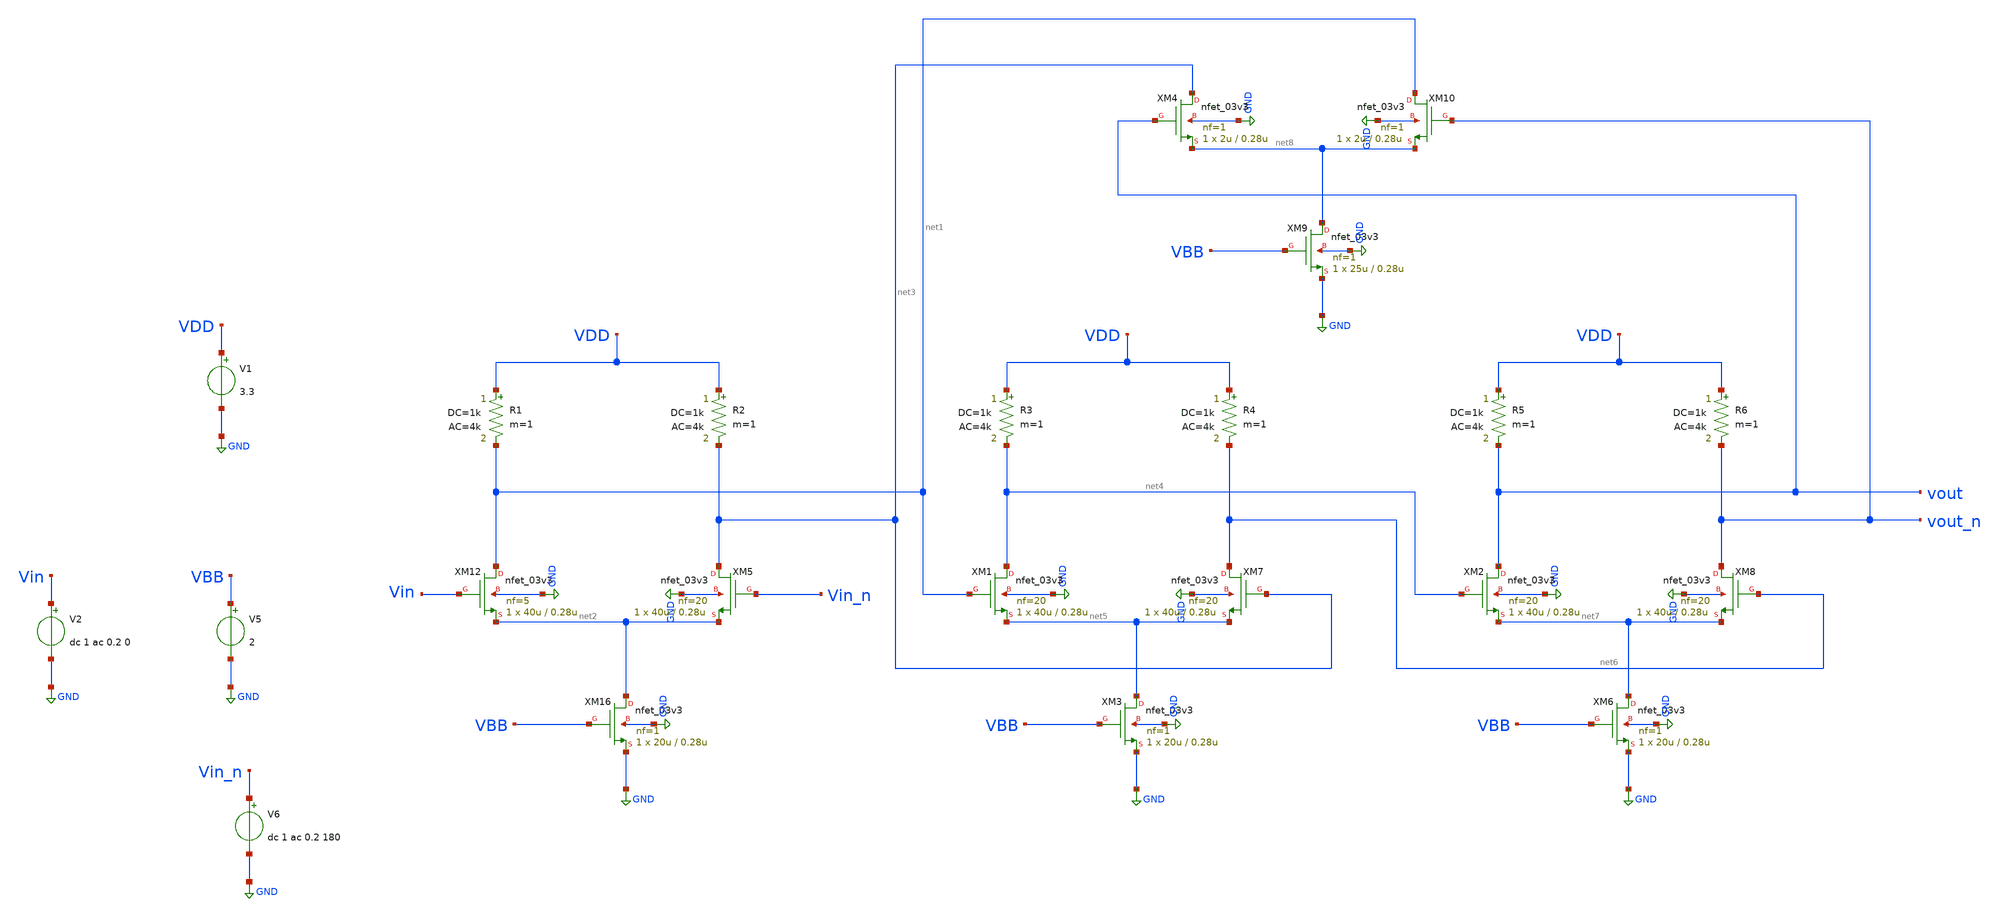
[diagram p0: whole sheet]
** sch_path: blocks/vga/fgas/untitled-4.sch
**.subckt untitled-4
XM12 net1 Vin net2 GND nfet_03v3 L=0.28u W=40u nf=5 ad='int((nf+1)/2) * W/nf * 0.18u' as='int((nf+2)/2) * W/nf * 0.18u'
+ pd='2*int((nf+1)/2) * (W/nf + 0.18u)' ps='2*int((nf+2)/2) * (W/nf + 0.18u)' nrd='0.18u / W' nrs='0.18u / W'
+ sa=0 sb=0 sd=0 m=1
XM16 net2 VBB GND GND nfet_03v3 L=0.28u W=20u nf=1 ad='int((nf+1)/2) * W/nf * 0.18u' as='int((nf+2)/2) * W/nf * 0.18u'
+ pd='2*int((nf+1)/2) * (W/nf + 0.18u)' ps='2*int((nf+2)/2) * (W/nf + 0.18u)' nrd='0.18u / W' nrs='0.18u / W'
+ sa=0 sb=0 sd=0 m=1
V1 VDD GND 3.3
V2 Vin GND dc 1 ac 0.2 0
V6 Vin_n GND dc 1 ac 0.2 180
V5 VBB GND 2
R1 VDD net1 1k ac=4k m=1
R2 VDD net3 1k ac=4k m=1
XM3 net5 VBB GND GND nfet_03v3 L=0.28u W=20u nf=1 ad='int((nf+1)/2) * W/nf * 0.18u' as='int((nf+2)/2) * W/nf * 0.18u'
+ pd='2*int((nf+1)/2) * (W/nf + 0.18u)' ps='2*int((nf+2)/2) * (W/nf + 0.18u)' nrd='0.18u / W' nrs='0.18u / W'
+ sa=0 sb=0 sd=0 m=1
R3 VDD net4 1k ac=4k m=1
R4 VDD net6 1k ac=4k m=1
XM6 net7 VBB GND GND nfet_03v3 L=0.28u W=20u nf=1 ad='int((nf+1)/2) * W/nf * 0.18u' as='int((nf+2)/2) * W/nf * 0.18u'
+ pd='2*int((nf+1)/2) * (W/nf + 0.18u)' ps='2*int((nf+2)/2) * (W/nf + 0.18u)' nrd='0.18u / W' nrs='0.18u / W'
+ sa=0 sb=0 sd=0 m=1
R5 VDD vout 1k ac=4k m=1
R6 VDD vout_n 1k ac=4k m=1
XM9 net8 VBB GND GND nfet_03v3 L=0.28u W=25u nf=1 ad='int((nf+1)/2) * W/nf * 0.18u' as='int((nf+2)/2) * W/nf * 0.18u'
+ pd='2*int((nf+1)/2) * (W/nf + 0.18u)' ps='2*int((nf+2)/2) * (W/nf + 0.18u)' nrd='0.18u / W' nrs='0.18u / W'
+ sa=0 sb=0 sd=0 m=1
XM1 net4 net1 net5 GND nfet_03v3 L=0.28u W=40u nf=20 ad='int((nf+1)/2) * W/nf * 0.18u' as='int((nf+2)/2) * W/nf * 0.18u'
+ pd='2*int((nf+1)/2) * (W/nf + 0.18u)' ps='2*int((nf+2)/2) * (W/nf + 0.18u)' nrd='0.18u / W' nrs='0.18u / W'
+ sa=0 sb=0 sd=0 m=1
XM2 vout net4 net7 GND nfet_03v3 L=0.28u W=40u nf=20 ad='int((nf+1)/2) * W/nf * 0.18u' as='int((nf+2)/2) * W/nf * 0.18u'
+ pd='2*int((nf+1)/2) * (W/nf + 0.18u)' ps='2*int((nf+2)/2) * (W/nf + 0.18u)' nrd='0.18u / W' nrs='0.18u / W'
+ sa=0 sb=0 sd=0 m=1
XM4 net3 vout net8 GND nfet_03v3 L=0.28u W=2u nf=1 ad='int((nf+1)/2) * W/nf * 0.18u' as='int((nf+2)/2) * W/nf * 0.18u'
+ pd='2*int((nf+1)/2) * (W/nf + 0.18u)' ps='2*int((nf+2)/2) * (W/nf + 0.18u)' nrd='0.18u / W' nrs='0.18u / W'
+ sa=0 sb=0 sd=0 m=1
XM5 net3 Vin_n net2 GND nfet_03v3 L=0.28u W=40u nf=20 ad='int((nf+1)/2) * W/nf * 0.18u' as='int((nf+2)/2) * W/nf * 0.18u'
+ pd='2*int((nf+1)/2) * (W/nf + 0.18u)' ps='2*int((nf+2)/2) * (W/nf + 0.18u)' nrd='0.18u / W' nrs='0.18u / W'
+ sa=0 sb=0 sd=0 m=1
XM7 net6 net3 net5 GND nfet_03v3 L=0.28u W=40u nf=20 ad='int((nf+1)/2) * W/nf * 0.18u' as='int((nf+2)/2) * W/nf * 0.18u'
+ pd='2*int((nf+1)/2) * (W/nf + 0.18u)' ps='2*int((nf+2)/2) * (W/nf + 0.18u)' nrd='0.18u / W' nrs='0.18u / W'
+ sa=0 sb=0 sd=0 m=1
XM8 vout_n net6 net7 GND nfet_03v3 L=0.28u W=40u nf=20 ad='int((nf+1)/2) * W/nf * 0.18u' as='int((nf+2)/2) * W/nf * 0.18u'
+ pd='2*int((nf+1)/2) * (W/nf + 0.18u)' ps='2*int((nf+2)/2) * (W/nf + 0.18u)' nrd='0.18u / W' nrs='0.18u / W'
+ sa=0 sb=0 sd=0 m=1
XM10 net1 vout_n net8 GND nfet_03v3 L=0.28u W=2u nf=1 ad='int((nf+1)/2) * W/nf * 0.18u' as='int((nf+2)/2) * W/nf * 0.18u'
+ pd='2*int((nf+1)/2) * (W/nf + 0.18u)' ps='2*int((nf+2)/2) * (W/nf + 0.18u)' nrd='0.18u / W' nrs='0.18u / W'
+ sa=0 sb=0 sd=0 m=1
**** begin user architecture code


.include /foss/pdks/gf180mcuD/libs.tech/ngspice/design.ngspice
.lib /foss/pdks/gf180mcuD/libs.tech/ngspice/sm141064.ngspice ss
.lib /foss/pdks/gf180mcuD/libs.tech/ngspice/sm141064.ngspice res_ss
.option method=gear

.control
save all
ac dec 40 1Meg 10G
let vdiff = v(vout) - v(vout_n)
let gain_db = db(vdiff)

meas ac maxgain MAX gain_db
meas ac f3db WHEN gain_db='maxgain-3' FALL=1

plot db(vdiff)

write {VGA_Gilb_cell.raw}
.endc


**** end user architecture code
**.ends
.GLOBAL GND
.end
